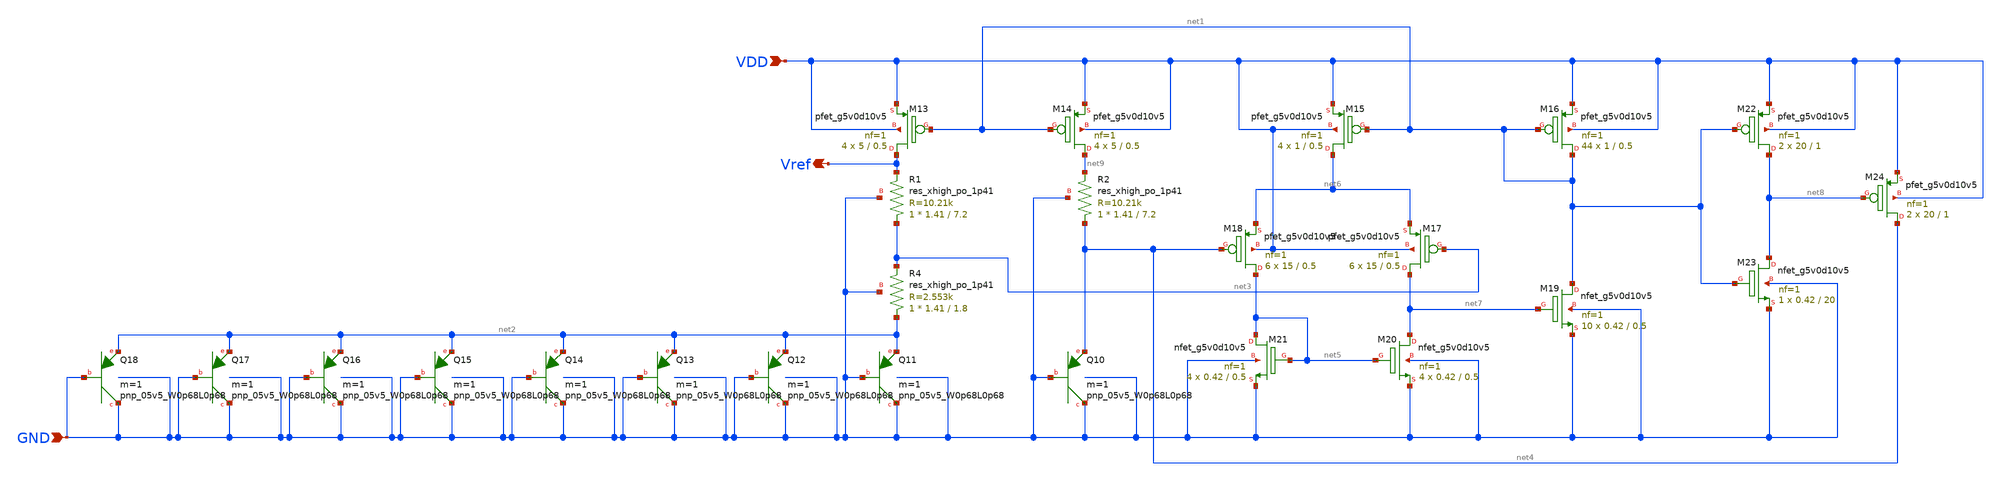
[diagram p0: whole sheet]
** sch_path: Analog_Blocks/Bandgap/Schematics/BGR1.8v_2/Bandgap_2.sch
**.subckt Bandgap_2 VDD GND Vref
*.ipin VDD
*.ipin GND
*.opin Vref
XM13 Vref net1 VDD VDD sky130_fd_pr__pfet_g5v0d10v5 L=0.5 W=5 nf=1 ad='int((nf+1)/2) * W/nf * 0.29' as='int((nf+2)/2) * W/nf * 0.29'
+ pd='2*int((nf+1)/2) * (W/nf + 0.29)' ps='2*int((nf+2)/2) * (W/nf + 0.29)' nrd='0.29 / W' nrs='0.29 / W'
+ sa=0 sb=0 sd=0 mult=4 m=4
XM14 net9 net1 VDD VDD sky130_fd_pr__pfet_g5v0d10v5 L=0.5 W=5 nf=1 ad='int((nf+1)/2) * W/nf * 0.29' as='int((nf+2)/2) * W/nf * 0.29'
+ pd='2*int((nf+1)/2) * (W/nf + 0.29)' ps='2*int((nf+2)/2) * (W/nf + 0.29)' nrd='0.29 / W' nrs='0.29 / W'
+ sa=0 sb=0 sd=0 mult=4 m=4
XQ10 GND GND net4 sky130_fd_pr__pnp_05v5_W0p68L0p68 m=1
XQ11 GND GND net2 sky130_fd_pr__pnp_05v5_W0p68L0p68 m=1
XQ12 GND GND net2 sky130_fd_pr__pnp_05v5_W0p68L0p68 m=1
XQ13 GND GND net2 sky130_fd_pr__pnp_05v5_W0p68L0p68 m=1
XQ14 GND GND net2 sky130_fd_pr__pnp_05v5_W0p68L0p68 m=1
XQ15 GND GND net2 sky130_fd_pr__pnp_05v5_W0p68L0p68 m=1
XQ16 GND GND net2 sky130_fd_pr__pnp_05v5_W0p68L0p68 m=1
XQ17 GND GND net2 sky130_fd_pr__pnp_05v5_W0p68L0p68 m=1
XQ18 GND GND net2 sky130_fd_pr__pnp_05v5_W0p68L0p68 m=1
XR4 net2 net3 GND sky130_fd_pr__res_xhigh_po_1p41 L=1.8 mult=1 m=1
XM15 net6 net1 VDD VDD sky130_fd_pr__pfet_g5v0d10v5 L=0.5 W=1 nf=1 ad='int((nf+1)/2) * W/nf * 0.29' as='int((nf+2)/2) * W/nf * 0.29'
+ pd='2*int((nf+1)/2) * (W/nf + 0.29)' ps='2*int((nf+2)/2) * (W/nf + 0.29)' nrd='0.29 / W' nrs='0.29 / W'
+ sa=0 sb=0 sd=0 mult=4 m=4
XM16 net1 net1 VDD VDD sky130_fd_pr__pfet_g5v0d10v5 L=0.5 W=1 nf=1 ad='int((nf+1)/2) * W/nf * 0.29' as='int((nf+2)/2) * W/nf * 0.29'
+ pd='2*int((nf+1)/2) * (W/nf + 0.29)' ps='2*int((nf+2)/2) * (W/nf + 0.29)' nrd='0.29 / W' nrs='0.29 / W'
+ sa=0 sb=0 sd=0 mult=44 m=44
XM17 net7 net3 net6 VDD sky130_fd_pr__pfet_g5v0d10v5 L=0.5 W=15 nf=1 ad='int((nf+1)/2) * W/nf * 0.29'
+ as='int((nf+2)/2) * W/nf * 0.29' pd='2*int((nf+1)/2) * (W/nf + 0.29)' ps='2*int((nf+2)/2) * (W/nf + 0.29)'
+ nrd='0.29 / W' nrs='0.29 / W' sa=0 sb=0 sd=0 mult=6 m=6
XM18 net5 net4 net6 VDD sky130_fd_pr__pfet_g5v0d10v5 L=0.5 W=15 nf=1 ad='int((nf+1)/2) * W/nf * 0.29'
+ as='int((nf+2)/2) * W/nf * 0.29' pd='2*int((nf+1)/2) * (W/nf + 0.29)' ps='2*int((nf+2)/2) * (W/nf + 0.29)'
+ nrd='0.29 / W' nrs='0.29 / W' sa=0 sb=0 sd=0 mult=6 m=6
XM19 net1 net7 GND GND sky130_fd_pr__nfet_g5v0d10v5 L=0.5 W=0.42 nf=1 ad='int((nf+1)/2) * W/nf * 0.29'
+ as='int((nf+2)/2) * W/nf * 0.29' pd='2*int((nf+1)/2) * (W/nf + 0.29)' ps='2*int((nf+2)/2) * (W/nf + 0.29)'
+ nrd='0.29 / W' nrs='0.29 / W' sa=0 sb=0 sd=0 mult=10 m=10
XM20 net7 net5 GND GND sky130_fd_pr__nfet_g5v0d10v5 L=0.5 W=0.42 nf=1 ad='int((nf+1)/2) * W/nf * 0.29'
+ as='int((nf+2)/2) * W/nf * 0.29' pd='2*int((nf+1)/2) * (W/nf + 0.29)' ps='2*int((nf+2)/2) * (W/nf + 0.29)'
+ nrd='0.29 / W' nrs='0.29 / W' sa=0 sb=0 sd=0 mult=4 m=4
XM21 net5 net5 GND GND sky130_fd_pr__nfet_g5v0d10v5 L=0.5 W=0.42 nf=1 ad='int((nf+1)/2) * W/nf * 0.29'
+ as='int((nf+2)/2) * W/nf * 0.29' pd='2*int((nf+1)/2) * (W/nf + 0.29)' ps='2*int((nf+2)/2) * (W/nf + 0.29)'
+ nrd='0.29 / W' nrs='0.29 / W' sa=0 sb=0 sd=0 mult=4 m=4
XM22 net8 net1 VDD VDD sky130_fd_pr__pfet_g5v0d10v5 L=1 W=20 nf=1 ad='int((nf+1)/2) * W/nf * 0.29' as='int((nf+2)/2) * W/nf * 0.29'
+ pd='2*int((nf+1)/2) * (W/nf + 0.29)' ps='2*int((nf+2)/2) * (W/nf + 0.29)' nrd='0.29 / W' nrs='0.29 / W'
+ sa=0 sb=0 sd=0 mult=2 m=2
XM23 net8 net1 GND GND sky130_fd_pr__nfet_g5v0d10v5 L=20 W=0.42 nf=1 ad='int((nf+1)/2) * W/nf * 0.29'
+ as='int((nf+2)/2) * W/nf * 0.29' pd='2*int((nf+1)/2) * (W/nf + 0.29)' ps='2*int((nf+2)/2) * (W/nf + 0.29)'
+ nrd='0.29 / W' nrs='0.29 / W' sa=0 sb=0 sd=0 mult=1 m=1
XM24 net4 net8 VDD VDD sky130_fd_pr__pfet_g5v0d10v5 L=1 W=20 nf=1 ad='int((nf+1)/2) * W/nf * 0.29' as='int((nf+2)/2) * W/nf * 0.29'
+ pd='2*int((nf+1)/2) * (W/nf + 0.29)' ps='2*int((nf+2)/2) * (W/nf + 0.29)' nrd='0.29 / W' nrs='0.29 / W'
+ sa=0 sb=0 sd=0 mult=2 m=2
XR1 net3 Vref GND sky130_fd_pr__res_xhigh_po_1p41 L=7.2 mult=1 m=1
XR2 net4 net9 GND sky130_fd_pr__res_xhigh_po_1p41 L=7.2 mult=1 m=1
**.ends
.end
